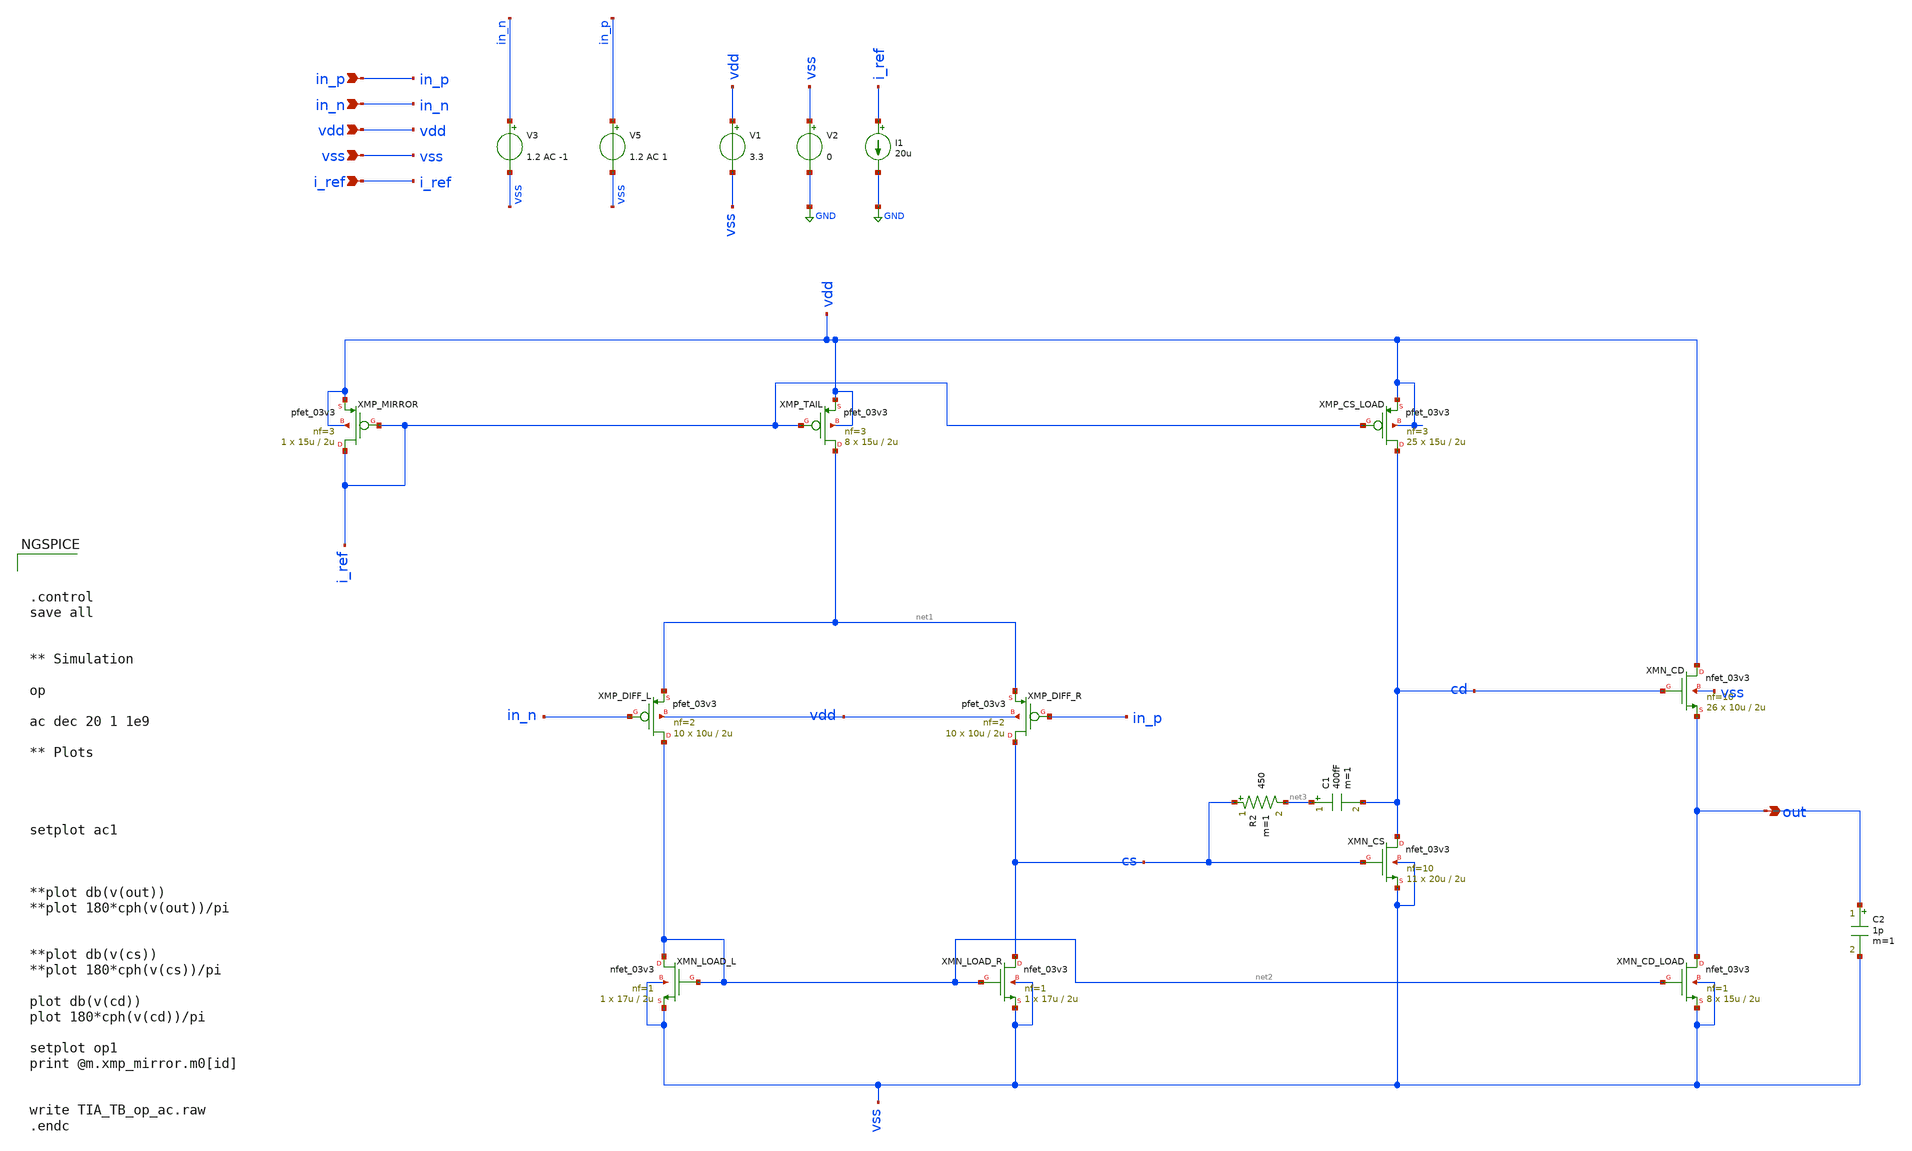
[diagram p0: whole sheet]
** sch_path: designs/libs/TIA/OLD_TB_TIA/TIA_TB_op_ac.sch
**.subckt TIA_TB_op_ac in_p in_n vdd vss i_ref out
*.ipin in_p
*.ipin in_n
*.ipin vdd
*.ipin vss
*.ipin i_ref
*.opin out
XMP_TAIL net1 i_ref vdd vdd pfet_03v3 L=2u W=15u nf=3 ad='int((nf+1)/2) * W/nf * 0.18u' as='int((nf+2)/2) * W/nf * 0.18u'
+ pd='2*int((nf+1)/2) * (W/nf + 0.18u)' ps='2*int((nf+2)/2) * (W/nf + 0.18u)' nrd='0.18u / W' nrs='0.18u / W'
+ sa=0 sb=0 sd=0 m=8
XMP_DIFF_L net2 in_n net1 vdd pfet_03v3 L=2u W=10u nf=2 ad='int((nf+1)/2) * W/nf * 0.18u' as='int((nf+2)/2) * W/nf * 0.18u'
+ pd='2*int((nf+1)/2) * (W/nf + 0.18u)' ps='2*int((nf+2)/2) * (W/nf + 0.18u)' nrd='0.18u / W' nrs='0.18u / W'
+ sa=0 sb=0 sd=0 m=10
XMP_DIFF_R cs in_p net1 vdd pfet_03v3 L=2u W=10u nf=2 ad='int((nf+1)/2) * W/nf * 0.18u' as='int((nf+2)/2) * W/nf * 0.18u'
+ pd='2*int((nf+1)/2) * (W/nf + 0.18u)' ps='2*int((nf+2)/2) * (W/nf + 0.18u)' nrd='0.18u / W' nrs='0.18u / W'
+ sa=0 sb=0 sd=0 m=10
XMP_CS_LOAD cd i_ref vdd vdd pfet_03v3 L=2u W=15u nf=3 ad='int((nf+1)/2) * W/nf * 0.18u' as='int((nf+2)/2) * W/nf * 0.18u'
+ pd='2*int((nf+1)/2) * (W/nf + 0.18u)' ps='2*int((nf+2)/2) * (W/nf + 0.18u)' nrd='0.18u / W' nrs='0.18u / W'
+ sa=0 sb=0 sd=0 m=25
XMP_MIRROR i_ref i_ref vdd vdd pfet_03v3 L=2u W=15u nf=3 ad='int((nf+1)/2) * W/nf * 0.18u' as='int((nf+2)/2) * W/nf * 0.18u'
+ pd='2*int((nf+1)/2) * (W/nf + 0.18u)' ps='2*int((nf+2)/2) * (W/nf + 0.18u)' nrd='0.18u / W' nrs='0.18u / W'
+ sa=0 sb=0 sd=0 m=1
XMN_LOAD_R cs net2 vss vss nfet_03v3 L=2u W=17u nf=1 ad='int((nf+1)/2) * W/nf * 0.18u' as='int((nf+2)/2) * W/nf * 0.18u'
+ pd='2*int((nf+1)/2) * (W/nf + 0.18u)' ps='2*int((nf+2)/2) * (W/nf + 0.18u)' nrd='0.18u / W' nrs='0.18u / W'
+ sa=0 sb=0 sd=0 m=1
XMN_LOAD_L net2 net2 vss vss nfet_03v3 L=2u W=17u nf=1 ad='int((nf+1)/2) * W/nf * 0.18u' as='int((nf+2)/2) * W/nf * 0.18u'
+ pd='2*int((nf+1)/2) * (W/nf + 0.18u)' ps='2*int((nf+2)/2) * (W/nf + 0.18u)' nrd='0.18u / W' nrs='0.18u / W'
+ sa=0 sb=0 sd=0 m=1
XMN_CS cd cs vss vss nfet_03v3 L=2u W=20u nf=10 ad='int((nf+1)/2) * W/nf * 0.18u' as='int((nf+2)/2) * W/nf * 0.18u'
+ pd='2*int((nf+1)/2) * (W/nf + 0.18u)' ps='2*int((nf+2)/2) * (W/nf + 0.18u)' nrd='0.18u / W' nrs='0.18u / W'
+ sa=0 sb=0 sd=0 m=11
XMN_CD vdd cd out vss nfet_03v3 L=2u W=10u nf=10 ad='int((nf+1)/2) * W/nf * 0.18u' as='int((nf+2)/2) * W/nf * 0.18u'
+ pd='2*int((nf+1)/2) * (W/nf + 0.18u)' ps='2*int((nf+2)/2) * (W/nf + 0.18u)' nrd='0.18u / W' nrs='0.18u / W'
+ sa=0 sb=0 sd=0 m=26
XMN_CD_LOAD out net2 vss vss nfet_03v3 L=2u W=15u nf=1 ad='int((nf+1)/2) * W/nf * 0.18u' as='int((nf+2)/2) * W/nf * 0.18u'
+ pd='2*int((nf+1)/2) * (W/nf + 0.18u)' ps='2*int((nf+2)/2) * (W/nf + 0.18u)' nrd='0.18u / W' nrs='0.18u / W'
+ sa=0 sb=0 sd=0 m=8
V1 vdd vss 3.3
C1 net3 cd 400fF m=1
R2 cs net3 450 m=1
V2 vss GND 0
V5 in_p vss 1.2 AC 1
I1 i_ref GND 20u
C2 out vss 1p m=1
V3 in_n vss 1.2 AC -1
**** begin user architecture code


.save @m.xmp_mirror.m0[gds]
.save @m.xmp_mirror.m0[gm]
.save @m.xmp_mirror.m0[id]
.save @m.xmp_mirror.m0[vth]
.save @m.xmp_mirror.m0[vdsat]
.save @m.xmp_mirror.m0[vds]


.save @m.xmp_tail.m0[gds]
.save @m.xmp_tail.m0[gm]
.save @m.xmp_tail.m0[id]
.save @m.xmp_tail.m0[vth]
.save @m.xmp_tail.m0[vdsat]
.save @m.xmp_tail.m0[vds]

.save @m.xmp_diff_l.m0[gds]
.save @m.xmp_diff_l.m0[gm]
.save @m.xmp_diff_l.m0[id]
.save @m.xmp_diff_l.m0[vth]
.save @m.xmp_diff_l.m0[vdsat]
.save @m.xmp_diff_l.m0[vds]

.save @m.xmp_diff_r.m0[gds]
.save @m.xmp_diff_r.m0[gm]
.save @m.xmp_diff_r.m0[id]
.save @m.xmp_diff_r.m0[vth]
.save @m.xmp_diff_r.m0[vdsat]
.save @m.xmp_diff_r.m0[vds]

.save @m.xmn_load_l.m0[gds]
.save @m.xmn_load_l.m0[gm]
.save @m.xmn_load_l.m0[id]
.save @m.xmn_load_l.m0[vth]
.save @m.xmn_load_l.m0[vdsat]
.save @m.xmn_load_l.m0[vds]

.save @m.xmn_load_r.m0[gds]
.save @m.xmn_load_r.m0[gm]
.save @m.xmn_load_r.m0[id]
.save @m.xmn_load_r.m0[vth]
.save @m.xmn_load_r.m0[vdsat]
.save @m.xmn_load_r.m0[vds]

.save @m.xmp_cs_load.m0[gds]
.save @m.xmp_cs_load.m0[gm]
.save @m.xmp_cs_load.m0[id]
.save @m.xmp_cs_load.m0[vth]
.save @m.xmp_cs_load.m0[vdsat]
.save @m.xmp_cs_load.m0[vds]

.save @m.xmn_cs.m0[gds]
.save @m.xmn_cs.m0[gm]
.save @m.xmn_cs.m0[id]
.save @m.xmn_cs.m0[vth]
.save @m.xmn_cs.m0[vdsat]
.save @m.xmn_cs.m0[vds]

.save @m.xmn_cd_load.m0[gds]
.save @m.xmn_cd_load.m0[gm]
.save @m.xmn_cd_load.m0[id]
.save @m.xmn_cd_load.m0[vth]
.save @m.xmn_cd_load.m0[vdsat]
.save @m.xmn_cd_load.m0[vds]

.save @m.xmn_cd.m0[gds]
.save @m.xmn_cd.m0[gm]
.save @m.xmn_cd.m0[id]
.save @m.xmn_cd.m0[vth]
.save @m.xmn_cd.m0[vdsat]
.save @m.xmn_cd.m0[vds]
.save @m.xmn_cd.m0[cgs]







.control
save all


** Simulation

op

ac dec 20 1 1e9

** Plots




setplot ac1



**plot db(v(out))
**plot 180*cph(v(out))/pi


**plot db(v(cs))
**plot 180*cph(v(cs))/pi

plot db(v(cd))
plot 180*cph(v(cd))/pi

setplot op1
print @m.xmp_mirror.m0[id]


write TIA_TB_op_ac.raw
.endc



.include $::180MCU_MODELS/design.ngspice
.lib $::180MCU_MODELS/sm141064.ngspice typical

**** end user architecture code
**.ends
.GLOBAL GND
.end
